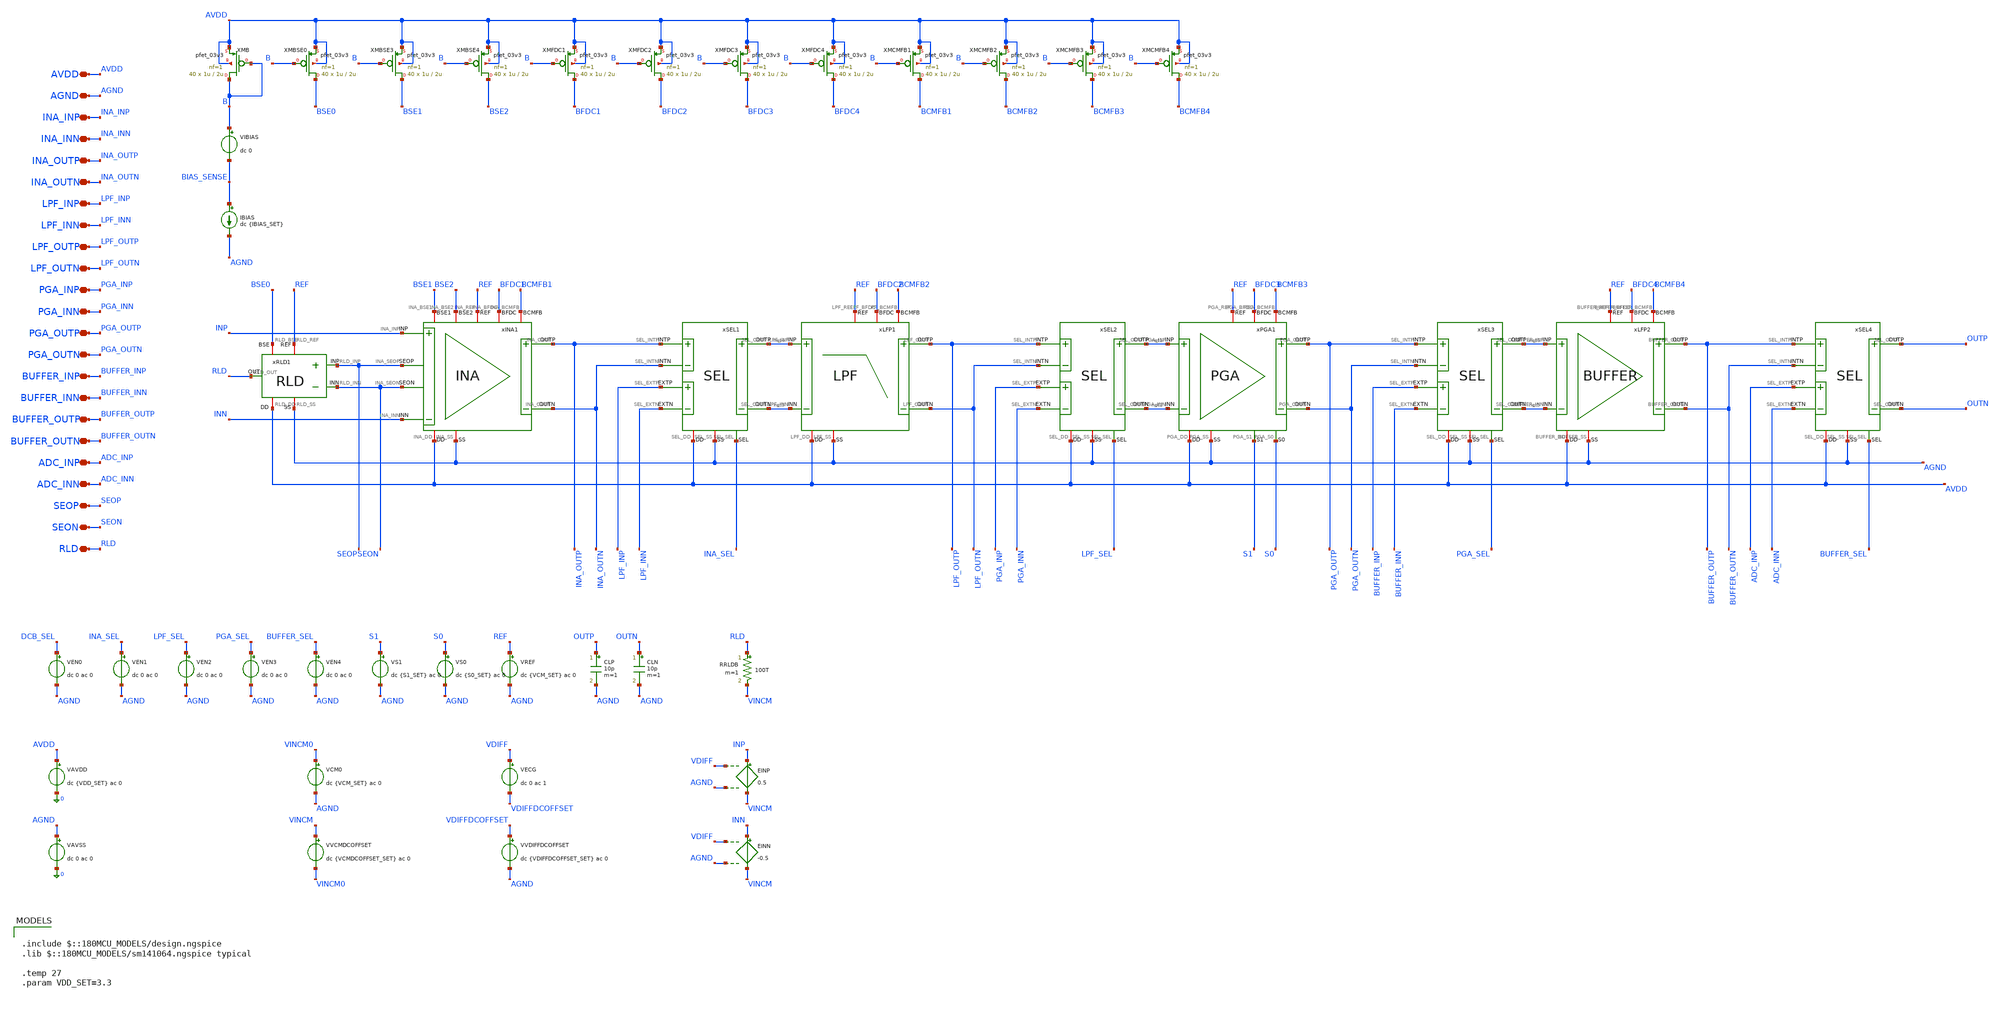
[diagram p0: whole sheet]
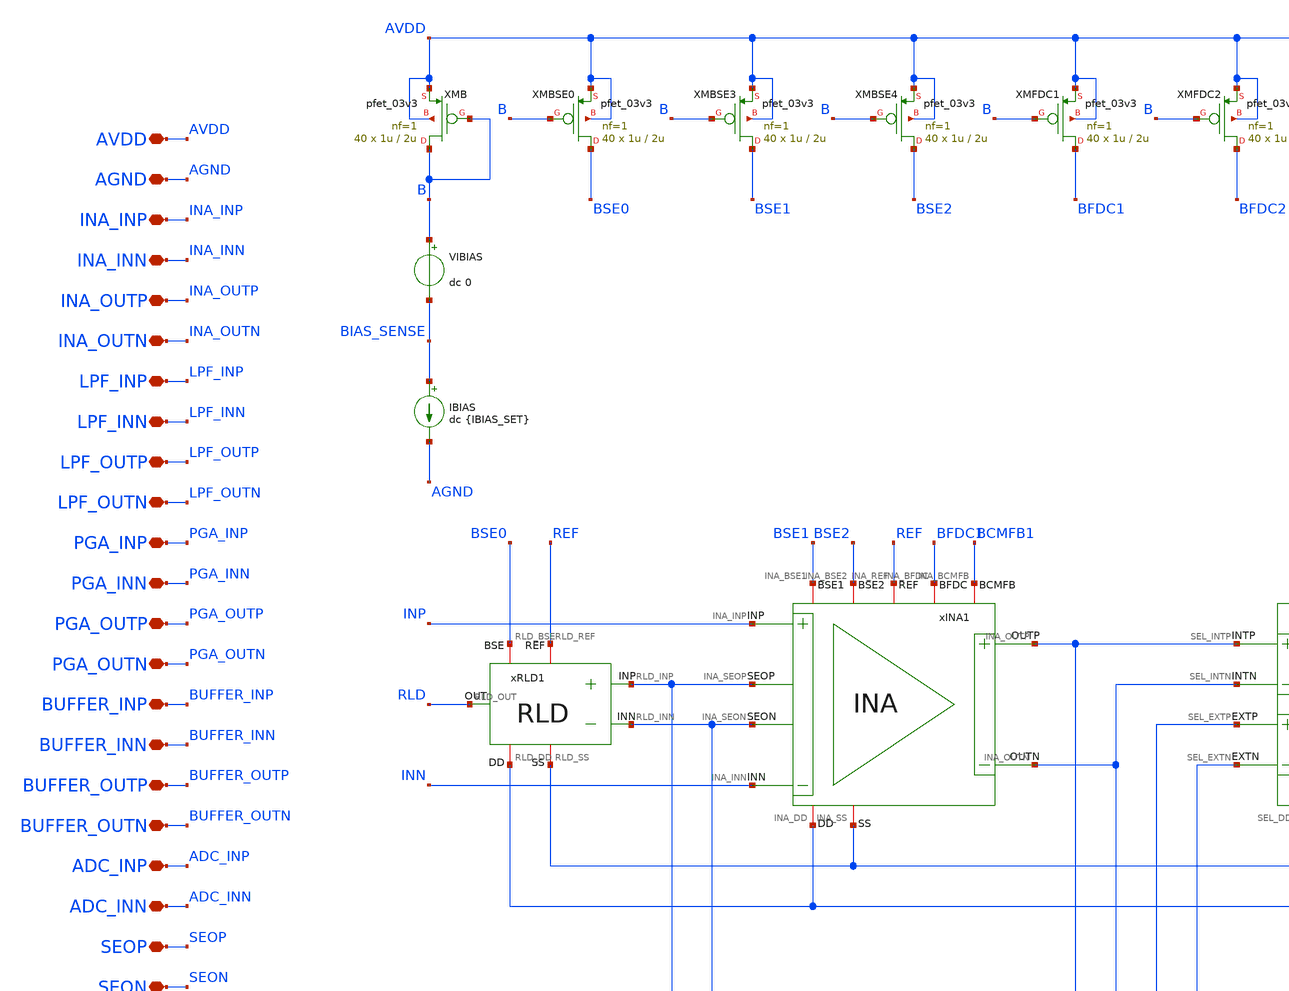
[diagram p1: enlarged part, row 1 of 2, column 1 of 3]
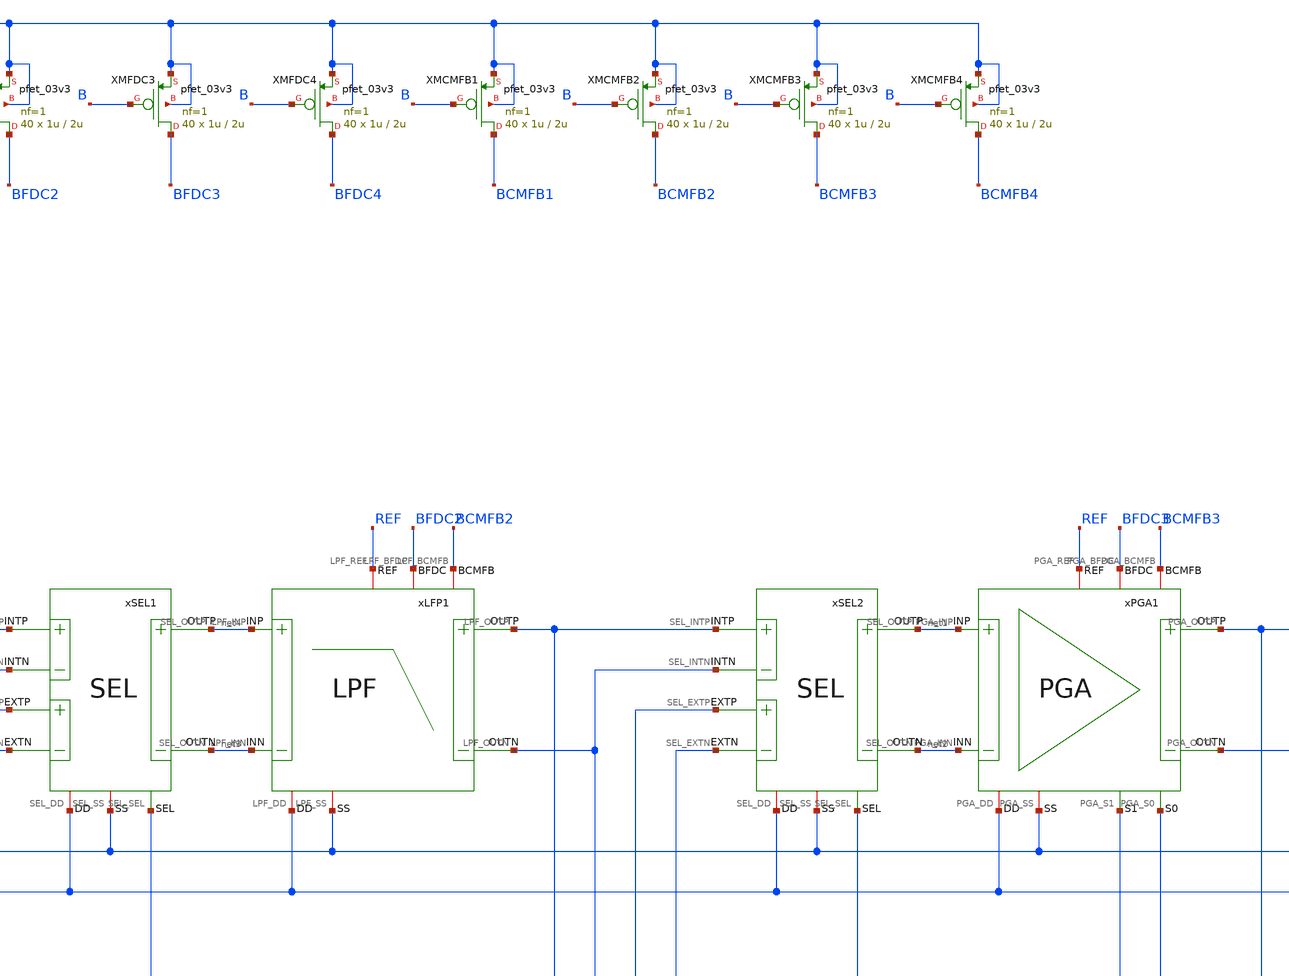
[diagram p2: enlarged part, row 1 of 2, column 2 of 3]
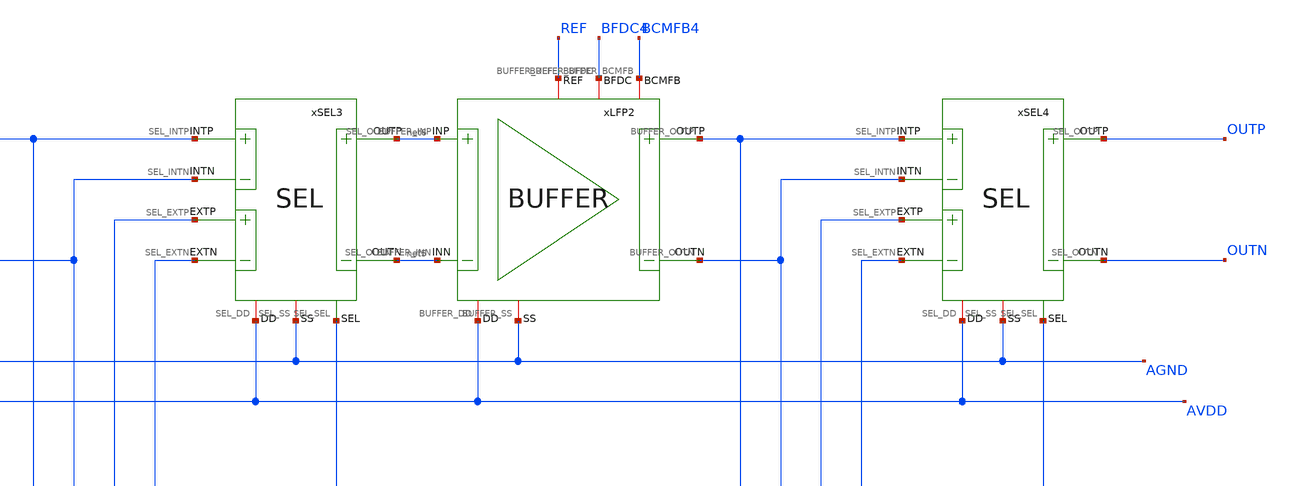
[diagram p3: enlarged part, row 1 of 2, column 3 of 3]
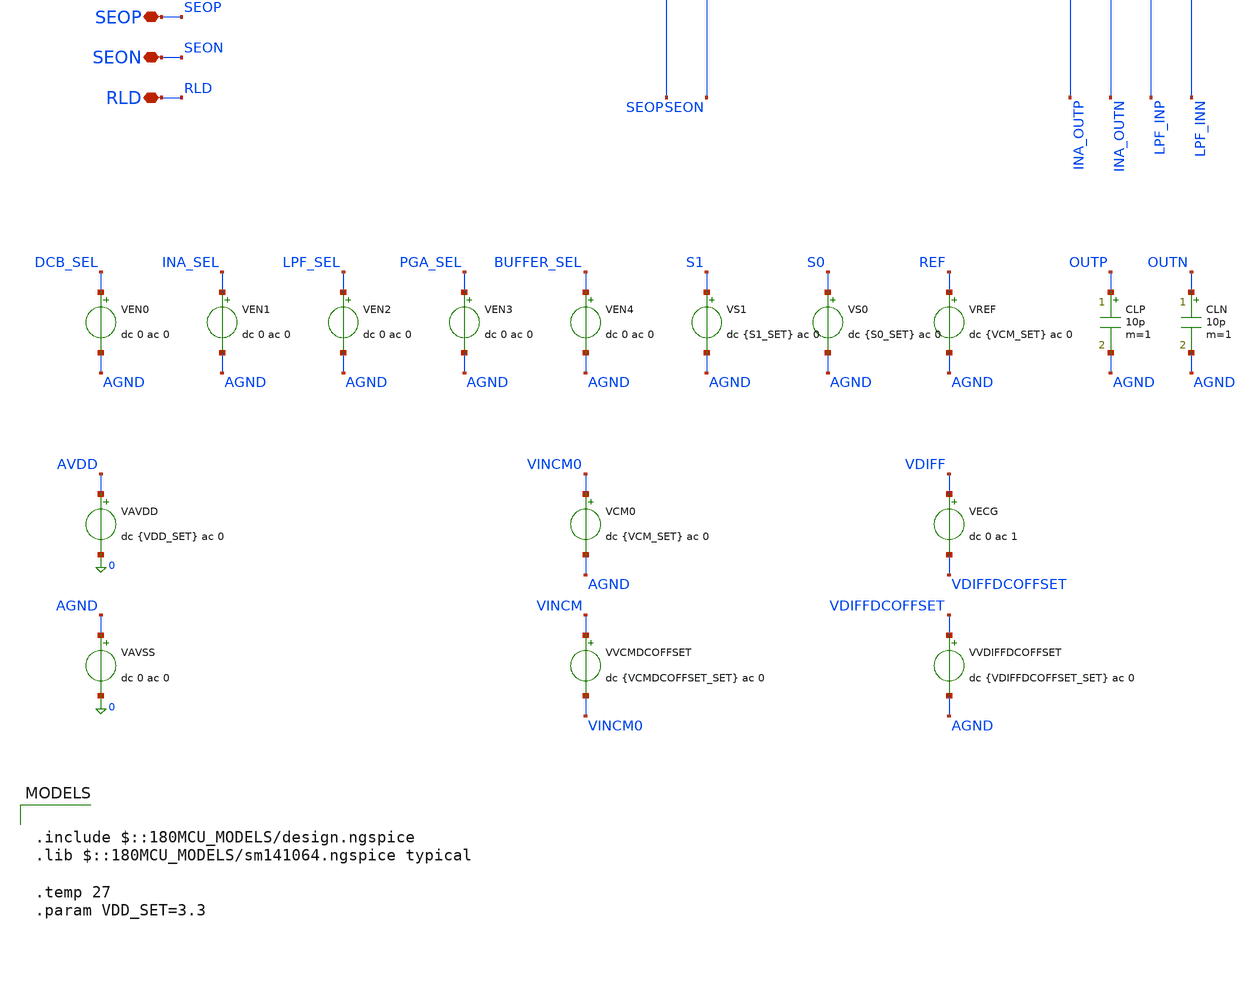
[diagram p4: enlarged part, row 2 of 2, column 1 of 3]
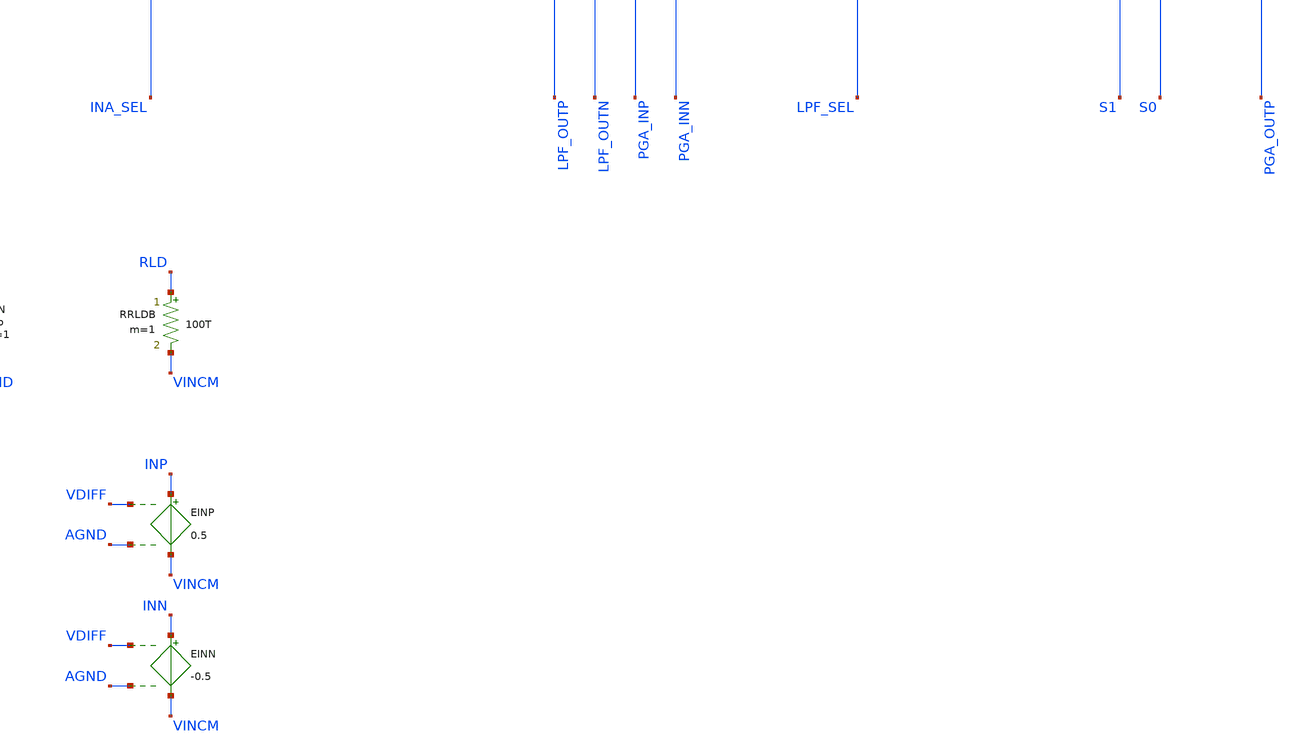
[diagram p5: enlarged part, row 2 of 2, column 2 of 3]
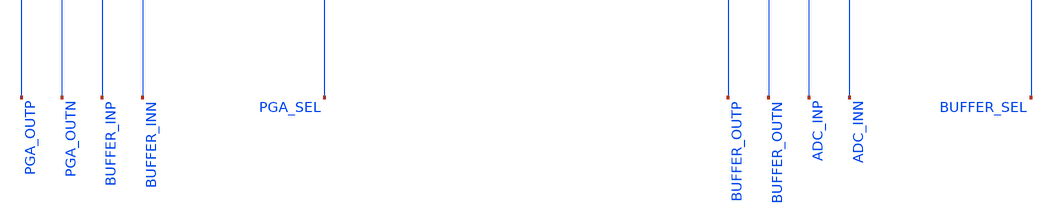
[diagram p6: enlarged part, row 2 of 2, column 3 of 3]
** sch_path: Design_Files/IC Design/Testbench/PATH/AC/PATH_TB_AC.sch
**.subckt PATH_TB_AC INA_INP INA_INN INA_OUTP INA_OUTN LPF_INP LPF_INN LPF_OUTP LPF_OUTN PGA_INP
*+ PGA_INN PGA_OUTP PGA_OUTN BUFFER_INP BUFFER_INN BUFFER_OUTP BUFFER_OUTN ADC_INP ADC_INN AVDD AGND SEOP SEON
*+ RLD
*.iopin INA_INP
*.iopin INA_INN
*.iopin INA_OUTP
*.iopin INA_OUTN
*.iopin LPF_INP
*.iopin LPF_INN
*.iopin LPF_OUTP
*.iopin LPF_OUTN
*.iopin PGA_INP
*.iopin PGA_INN
*.iopin PGA_OUTP
*.iopin PGA_OUTN
*.iopin BUFFER_INP
*.iopin BUFFER_INN
*.iopin BUFFER_OUTP
*.iopin BUFFER_OUTN
*.iopin ADC_INP
*.iopin ADC_INN
*.iopin AVDD
*.iopin AGND
*.iopin SEOP
*.iopin SEON
*.iopin RLD
CLP OUTP AGND 10p m=1
CLN OUTN AGND 10p m=1
VREF REF AGND dc {VCM_SET} ac 0
VEN1 INA_SEL AGND dc 0 ac 0
.save i(ven1)
VS0 S0 AGND dc {S0_SET} ac 0
VS1 S1 AGND dc {S1_SET} ac 0
VEN2 LPF_SEL AGND dc 0 ac 0
.save i(ven2)
VEN3 PGA_SEL AGND dc 0 ac 0
.save i(ven3)
VEN4 BUFFER_SEL AGND dc 0 ac 0
.save i(ven4)
VEN0 DCB_SEL AGND dc 0 ac 0
.save i(ven0)
VAVDD AVDD 0 dc {VDD_SET} ac 0
.save i(vavdd)
VAVSS AGND 0 dc 0 ac 0
.save i(vavss)
VCM0 VINCM0 AGND dc {VCM_SET} ac 0
VVCMDCOFFSET VINCM VINCM0 dc {VCMDCOFFSET_SET} ac 0
VECG VDIFF VDIFFDCOFFSET dc 0 ac 1
VVDIFFDCOFFSET VDIFFDCOFFSET AGND dc {VDIFFDCOFFSET_SET} ac 0
EINP INP VINCM VDIFF AGND 0.5
EINN INN VINCM VDIFF AGND -0.5
RRLDB RLD VINCM 100T m=1
VIBIAS B BIAS_SENSE dc 0
.save i(vibias)
IBIAS BIAS_SENSE AGND dc {IBIAS_SET}
xLFP1 AVDD AGND net4 net3 LPF_OUTN BFDC2 LPF_OUTP BCMFB2 REF LPF
xPGA1 AVDD AGND net1 net2 PGA_OUTN BFDC3 PGA_OUTP BCMFB3 REF S1 S0 PGA
xSEL1 AVDD AGND INA_OUTP INA_OUTN net3 net4 LPF_INP LPF_INN INA_SEL SEL
xINA1 AVDD AGND INP INN INA_OUTN BFDC1 INA_OUTP BCMFB1 REF SEON SEOP BSE1 BSE2 INA
xSEL2 AVDD AGND LPF_OUTP LPF_OUTN net2 net1 PGA_INP PGA_INN LPF_SEL SEL
xSEL3 AVDD AGND PGA_OUTP PGA_OUTN net5 net6 BUFFER_INP BUFFER_INN PGA_SEL SEL
xSEL4 AVDD AGND BUFFER_OUTP BUFFER_OUTN OUTN OUTP ADC_INP ADC_INN BUFFER_SEL SEL
xLFP2 AVDD AGND net6 net5 BUFFER_OUTN BFDC4 BUFFER_OUTP BCMFB4 REF BUFFER
XMB B B AVDD AVDD pfet_03v3 L=2u W=1u nf=1 ad='int((nf+1)/2) * W/nf * 0.18u' as='int((nf+2)/2) * W/nf * 0.18u'
+ pd='2*int((nf+1)/2) * (W/nf + 0.18u)' ps='2*int((nf+2)/2) * (W/nf + 0.18u)' nrd='0.18u / W' nrs='0.18u / W'
+ sa=0 sb=0 sd=0 m=40
XMBSE3 BSE1 B AVDD AVDD pfet_03v3 L=2u W=1u nf=1 ad='int((nf+1)/2) * W/nf * 0.18u' as='int((nf+2)/2) * W/nf * 0.18u'
+ pd='2*int((nf+1)/2) * (W/nf + 0.18u)' ps='2*int((nf+2)/2) * (W/nf + 0.18u)' nrd='0.18u / W' nrs='0.18u / W'
+ sa=0 sb=0 sd=0 m=40
XMBSE4 BSE2 B AVDD AVDD pfet_03v3 L=2u W=1u nf=1 ad='int((nf+1)/2) * W/nf * 0.18u' as='int((nf+2)/2) * W/nf * 0.18u'
+ pd='2*int((nf+1)/2) * (W/nf + 0.18u)' ps='2*int((nf+2)/2) * (W/nf + 0.18u)' nrd='0.18u / W' nrs='0.18u / W'
+ sa=0 sb=0 sd=0 m=40
XMFDC1 BFDC1 B AVDD AVDD pfet_03v3 L=2u W=1u nf=1 ad='int((nf+1)/2) * W/nf * 0.18u' as='int((nf+2)/2) * W/nf * 0.18u'
+ pd='2*int((nf+1)/2) * (W/nf + 0.18u)' ps='2*int((nf+2)/2) * (W/nf + 0.18u)' nrd='0.18u / W' nrs='0.18u / W'
+ sa=0 sb=0 sd=0 m=40
XMFDC2 BFDC2 B AVDD AVDD pfet_03v3 L=2u W=1u nf=1 ad='int((nf+1)/2) * W/nf * 0.18u' as='int((nf+2)/2) * W/nf * 0.18u'
+ pd='2*int((nf+1)/2) * (W/nf + 0.18u)' ps='2*int((nf+2)/2) * (W/nf + 0.18u)' nrd='0.18u / W' nrs='0.18u / W'
+ sa=0 sb=0 sd=0 m=40
XMFDC3 BFDC3 B AVDD AVDD pfet_03v3 L=2u W=1u nf=1 ad='int((nf+1)/2) * W/nf * 0.18u' as='int((nf+2)/2) * W/nf * 0.18u'
+ pd='2*int((nf+1)/2) * (W/nf + 0.18u)' ps='2*int((nf+2)/2) * (W/nf + 0.18u)' nrd='0.18u / W' nrs='0.18u / W'
+ sa=0 sb=0 sd=0 m=40
XMFDC4 BFDC4 B AVDD AVDD pfet_03v3 L=2u W=1u nf=1 ad='int((nf+1)/2) * W/nf * 0.18u' as='int((nf+2)/2) * W/nf * 0.18u'
+ pd='2*int((nf+1)/2) * (W/nf + 0.18u)' ps='2*int((nf+2)/2) * (W/nf + 0.18u)' nrd='0.18u / W' nrs='0.18u / W'
+ sa=0 sb=0 sd=0 m=40
XMCMFB1 BCMFB1 B AVDD AVDD pfet_03v3 L=2u W=1u nf=1 ad='int((nf+1)/2) * W/nf * 0.18u' as='int((nf+2)/2) * W/nf * 0.18u'
+ pd='2*int((nf+1)/2) * (W/nf + 0.18u)' ps='2*int((nf+2)/2) * (W/nf + 0.18u)' nrd='0.18u / W' nrs='0.18u / W'
+ sa=0 sb=0 sd=0 m=40
XMCMFB2 BCMFB2 B AVDD AVDD pfet_03v3 L=2u W=1u nf=1 ad='int((nf+1)/2) * W/nf * 0.18u' as='int((nf+2)/2) * W/nf * 0.18u'
+ pd='2*int((nf+1)/2) * (W/nf + 0.18u)' ps='2*int((nf+2)/2) * (W/nf + 0.18u)' nrd='0.18u / W' nrs='0.18u / W'
+ sa=0 sb=0 sd=0 m=40
XMCMFB3 BCMFB3 B AVDD AVDD pfet_03v3 L=2u W=1u nf=1 ad='int((nf+1)/2) * W/nf * 0.18u' as='int((nf+2)/2) * W/nf * 0.18u'
+ pd='2*int((nf+1)/2) * (W/nf + 0.18u)' ps='2*int((nf+2)/2) * (W/nf + 0.18u)' nrd='0.18u / W' nrs='0.18u / W'
+ sa=0 sb=0 sd=0 m=40
XMCMFB4 BCMFB4 B AVDD AVDD pfet_03v3 L=2u W=1u nf=1 ad='int((nf+1)/2) * W/nf * 0.18u' as='int((nf+2)/2) * W/nf * 0.18u'
+ pd='2*int((nf+1)/2) * (W/nf + 0.18u)' ps='2*int((nf+2)/2) * (W/nf + 0.18u)' nrd='0.18u / W' nrs='0.18u / W'
+ sa=0 sb=0 sd=0 m=40
XMBSE0 BSE0 B AVDD AVDD pfet_03v3 L=2u W=1u nf=1 ad='int((nf+1)/2) * W/nf * 0.18u' as='int((nf+2)/2) * W/nf * 0.18u'
+ pd='2*int((nf+1)/2) * (W/nf + 0.18u)' ps='2*int((nf+2)/2) * (W/nf + 0.18u)' nrd='0.18u / W' nrs='0.18u / W'
+ sa=0 sb=0 sd=0 m=40
xRLD1 AVDD AGND SEOP SEON RLD REF BSE0 RLD
**** begin user architecture code

.include $::180MCU_MODELS/design.ngspice
.lib $::180MCU_MODELS/sm141064.ngspice typical

.temp 27
.param VDD_SET=3.3



.param VCM_SET={VDD_SET/2}

.param VCMDCOFFSET_SET=0
.param VDIFFDCOFFSET_SET=0

.param IBIAS_SET=40u

.param S1_SET=3.3
.param S0_SET=3.3

.options method=gear
.options sparse

.options gmin=1e-12
.options rshunt=100T

.options reltol=1e-3
.options abstol=1e-12
.options vntol=1u
.options chgtol=1e-14

.options itl1=2000
.options itl2=1000
.options itl4=2000

.nodeset v(B)=2.3

.nodeset v(INP)={VCM_SET}
.nodeset v(INN)={VCM_SET}

.nodeset v(DCB_OUTP)={VCM_SET}
.nodeset v(DCB_OUTN)={VCM_SET}

.nodeset v(INA_OUTP)={VCM_SET}
.nodeset v(INA_OUTN)={VCM_SET}

.nodeset v(LPF_OUTP)={VCM_SET}
.nodeset v(LPF_OUTN)={VCM_SET}

.nodeset v(PGA_OUTP)={VCM_SET}
.nodeset v(PGA_OUTN)={VCM_SET}

.nodeset v(BUFFER_OUTP)={VCM_SET}
.nodeset v(BUFFER_OUTN)={VCM_SET}

.nodeset v(OUTP)={VCM_SET}
.nodeset v(OUTN)={VCM_SET}

.nodeset v(RLD)={VCM_SET}

.save all





.control

destroy all

set noaskquit
set wr_singlescale
unset wr_vecnames
set appendwrite
set units=degrees

option numdgt=15
option sparse

shell mkdir -p
+ /foss/designs/ECG_Acquisition_IC/Measurement_Results/IC_Simulation/PATH/NOM.Result_txt

shell rm -f
+ /foss/designs/ECG_Acquisition_IC/Measurement_Results/IC_Simulation/PATH/NOM.Result_txt/NOM.op.txt
shell rm -f
+ /foss/designs/ECG_Acquisition_IC/Measurement_Results/IC_Simulation/PATH/NOM.Result_txt/NOM.diff_ac.txt
shell rm -f
+ /foss/designs/ECG_Acquisition_IC/Measurement_Results/IC_Simulation/PATH/NOM.Result_txt/NOM.cmrr_ac.txt
shell rm -f
+ /foss/designs/ECG_Acquisition_IC/Measurement_Results/IC_Simulation/PATH/NOM.Result_txt/NOM.psrrp_ac.txt
shell rm -f
+ /foss/designs/ECG_Acquisition_IC/Measurement_Results/IC_Simulation/PATH/NOM.Result_txt/NOM.psrrn_ac.txt


* OP: G2 and G16
foreach gaincfg 0 1

    if $gaincfg = 0
        alterparam S1_SET=0
        alterparam S0_SET=0
    else
        alterparam S1_SET=3.3
        alterparam S0_SET=3.3
    end

    reset
    save all

    alter @VECG[ACMAG]=0
    alter @VECG[ACPHASE]=0

    alter @VCM0[ACMAG]=0
    alter @VCM0[ACPHASE]=0

    alter @VAVDD[ACMAG]=0
    alter @VAVDD[ACPHASE]=0

    alter @VAVSS[ACMAG]=0
    alter @VAVSS[ACPHASE]=0

    op

    let op_index=0

    if $gaincfg = 0
        let op_pga_gain=op_index*0+2
    else
        let op_pga_gain=op_index*0+16
    end

    let op_vdd=v(AVDD)-v(AGND)

    let op_vinp=v(INP)-v(AGND)
    let op_vinn=v(INN)-v(AGND)

    let op_vin_cm=0.5*(v(INP)+v(INN))-v(AGND)
    let op_vin_diff=v(INP)-v(INN)

    let op_outp=v(OUTP)-v(AGND)
    let op_outn=v(OUTN)-v(AGND)

    let op_vout_cm=0.5*(v(OUTP)+v(OUTN))-v(AGND)
    let op_vout_diff=v(OUTP)-v(OUTN)

    let op_rld=v(RLD)-v(AGND)
    let op_ref=v(REF)-v(AGND)

    let op_ibias=abs(vibias#branch)
    let op_idd=abs(vavdd#branch)
    let op_power=op_vdd*op_idd

    setscale op_index

    wrdata
+ /foss/designs/ECG_Acquisition_IC/Measurement_Results/IC_Simulation/PATH/NOM.Result_txt/NOM.op.txt op_pga_gain op_vdd op_vinp op_vinn op_vin_cm op_vin_diff op_outp op_outn op_vout_cm op_vout_diff
+ op_rld op_ref op_ibias op_idd op_power

    destroy $curplot

end


* Differential AC: G2 and G16
foreach gaincfg 0 1

    if $gaincfg = 0
        alterparam S1_SET=0
        alterparam S0_SET=0
    else
        alterparam S1_SET=3.3
        alterparam S0_SET=3.3
    end

    reset
    save all

    alter @VECG[ACMAG]=1
    alter @VECG[ACPHASE]=0

    alter @VCM0[ACMAG]=0
    alter @VCM0[ACPHASE]=0

    alter @VAVDD[ACMAG]=0
    alter @VAVDD[ACPHASE]=0

    alter @VAVSS[ACMAG]=0
    alter @VAVSS[ACPHASE]=0

    ac dec 200 0.001 10k

    if $gaincfg = 0
        let ac_pga_gain=frequency*0+2
    else
        let ac_pga_gain=frequency*0+16
    end

    let ac_vin_diff=v(INP)-v(INN)
    let ac_vout_diff=v(OUTP)-v(OUTN)
    let ac_vout_cm=0.5*(v(OUTP)+v(OUTN))-v(AGND)

    let ac_hdiff=ac_vout_diff/ac_vin_diff

    let vin_diff_real=real(ac_vin_diff)
    let vin_diff_imag=imag(ac_vin_diff)
    let vin_diff_mag=mag(ac_vin_diff)
    let vin_diff_phase=ph(ac_vin_diff)

    let vout_diff_real=real(ac_vout_diff)
    let vout_diff_imag=imag(ac_vout_diff)
    let vout_diff_mag=mag(ac_vout_diff)
    let vout_diff_phase=ph(ac_vout_diff)

    let vout_cm_real=real(ac_vout_cm)
    let vout_cm_imag=imag(ac_vout_cm)

    let hdiff_real=real(ac_hdiff)
    let hdiff_imag=imag(ac_hdiff)
    let hdiff_mag=mag(ac_hdiff)
    let hdiff_db=db(ac_hdiff)
    let hdiff_phase=ph(ac_hdiff)

    setscale frequency

    wrdata
+ /foss/designs/ECG_Acquisition_IC/Measurement_Results/IC_Simulation/PATH/NOM.Result_txt/NOM.diff_ac.txt ac_pga_gain vin_diff_real vin_diff_imag vin_diff_mag vin_diff_phase vout_diff_real vout_diff_imag
+ vout_diff_mag vout_diff_phase vout_cm_real vout_cm_imag hdiff_real hdiff_imag hdiff_mag hdiff_db hdiff_phase

    destroy $curplot

end


* CMRR AC: G2 and G16
foreach gaincfg 0 1

    if $gaincfg = 0
        alterparam S1_SET=0
        alterparam S0_SET=0
    else
        alterparam S1_SET=3.3
        alterparam S0_SET=3.3
    end

    reset
    save all

    alter @VECG[ACMAG]=0
    alter @VECG[ACPHASE]=0

    alter @VCM0[ACMAG]=1
    alter @VCM0[ACPHASE]=0

    alter @VAVDD[ACMAG]=0
    alter @VAVDD[ACPHASE]=0

    alter @VAVSS[ACMAG]=0
    alter @VAVSS[ACPHASE]=0

    ac dec 200 0.001 10k

    if $gaincfg = 0
        let ac_pga_gain=frequency*0+2
    else
        let ac_pga_gain=frequency*0+16
    end

    let ac_vin_cm=0.5*(v(INP)+v(INN))-v(AGND)
    let ac_vout_diff=v(OUTP)-v(OUTN)
    let ac_vout_cm=0.5*(v(OUTP)+v(OUTN))-v(AGND)

    let ac_hcm_diff=ac_vout_diff/ac_vin_cm

    let vin_cm_real=real(ac_vin_cm)
    let vin_cm_imag=imag(ac_vin_cm)
    let vin_cm_mag=mag(ac_vin_cm)
    let vin_cm_phase=ph(ac_vin_cm)

    let vout_diff_real=real(ac_vout_diff)
    let vout_diff_imag=imag(ac_vout_diff)

    let vout_cm_real=real(ac_vout_cm)
    let vout_cm_imag=imag(ac_vout_cm)

    let hcm_diff_real=real(ac_hcm_diff)
    let hcm_diff_imag=imag(ac_hcm_diff)
    let hcm_diff_mag=mag(ac_hcm_diff)
    let hcm_diff_db=db(ac_hcm_diff)
    let hcm_diff_phase=ph(ac_hcm_diff)

    setscale frequency

    wrdata
+ /foss/designs/ECG_Acquisition_IC/Measurement_Results/IC_Simulation/PATH/NOM.Result_txt/NOM.cmrr_ac.txt ac_pga_gain vin_cm_real vin_cm_imag vin_cm_mag vin_cm_phase vout_diff_real vout_diff_imag
+ vout_cm_real vout_cm_imag hcm_diff_real hcm_diff_imag hcm_diff_mag hcm_diff_db hcm_diff_phase

    destroy $curplot

end


* PSRR+ AC: G2 and G16
foreach gaincfg 0 1

    if $gaincfg = 0
        alterparam S1_SET=0
        alterparam S0_SET=0
    else
        alterparam S1_SET=3.3
        alterparam S0_SET=3.3
    end

    reset
    save all

    alter @VECG[ACMAG]=0
    alter @VECG[ACPHASE]=0

    alter @VCM0[ACMAG]=0
    alter @VCM0[ACPHASE]=0

    alter @VAVDD[ACMAG]=1
    alter @VAVDD[ACPHASE]=0

    alter @VAVSS[ACMAG]=0
    alter @VAVSS[ACPHASE]=0

    ac dec 200 0.001 10k

    if $gaincfg = 0
        let ac_pga_gain=frequency*0+2
    else
        let ac_pga_gain=frequency*0+16
    end

    let ac_supply=v(AVDD)-v(AGND)
    let ac_vout_diff=v(OUTP)-v(OUTN)
    let ac_vout_cm=0.5*(v(OUTP)+v(OUTN))-v(AGND)

    let ac_hpsrrp=ac_vout_diff/ac_supply

    let supply_real=real(ac_supply)
    let supply_imag=imag(ac_supply)
    let supply_mag=mag(ac_supply)
    let supply_phase=ph(ac_supply)

    let vout_diff_real=real(ac_vout_diff)
    let vout_diff_imag=imag(ac_vout_diff)

    let vout_cm_real=real(ac_vout_cm)
    let vout_cm_imag=imag(ac_vout_cm)

    let hpsrrp_real=real(ac_hpsrrp)
    let hpsrrp_imag=imag(ac_hpsrrp)
    let hpsrrp_mag=mag(ac_hpsrrp)
    let hpsrrp_db=db(ac_hpsrrp)
    let hpsrrp_phase=ph(ac_hpsrrp)

    setscale frequency

    wrdata
+ /foss/designs/ECG_Acquisition_IC/Measurement_Results/IC_Simulation/PATH/NOM.Result_txt/NOM.psrrp_ac.txt ac_pga_gain supply_real supply_imag supply_mag supply_phase vout_diff_real vout_diff_imag
+ vout_cm_real vout_cm_imag hpsrrp_real hpsrrp_imag hpsrrp_mag hpsrrp_db hpsrrp_phase

    destroy $curplot

end


* PSRR- AC: G2 and G16
foreach gaincfg 0 1

    if $gaincfg = 0
        alterparam S1_SET=0
        alterparam S0_SET=0
    else
        alterparam S1_SET=3.3
        alterparam S0_SET=3.3
    end

    reset
    save all

    alter @VECG[ACMAG]=0
    alter @VECG[ACPHASE]=0

    alter @VCM0[ACMAG]=0
    alter @VCM0[ACPHASE]=0

    alter @VAVDD[ACMAG]=0
    alter @VAVDD[ACPHASE]=0

    alter @VAVSS[ACMAG]=1
    alter @VAVSS[ACPHASE]=0

    ac dec 200 0.001 10k

    if $gaincfg = 0
        let ac_pga_gain=frequency*0+2
    else
        let ac_pga_gain=frequency*0+16
    end

    let ac_supply=v(AGND)
    let ac_vout_diff=v(OUTP)-v(OUTN)
    let ac_vout_cm=0.5*(v(OUTP)+v(OUTN))-v(AGND)

    let ac_hpsrrn=ac_vout_diff/ac_supply

    let supply_real=real(ac_supply)
    let supply_imag=imag(ac_supply)
    let supply_mag=mag(ac_supply)
    let supply_phase=ph(ac_supply)

    let vout_diff_real=real(ac_vout_diff)
    let vout_diff_imag=imag(ac_vout_diff)

    let vout_cm_real=real(ac_vout_cm)
    let vout_cm_imag=imag(ac_vout_cm)

    let hpsrrn_real=real(ac_hpsrrn)
    let hpsrrn_imag=imag(ac_hpsrrn)
    let hpsrrn_mag=mag(ac_hpsrrn)
    let hpsrrn_db=db(ac_hpsrrn)
    let hpsrrn_phase=ph(ac_hpsrrn)

    setscale frequency

    wrdata
+ /foss/designs/ECG_Acquisition_IC/Measurement_Results/IC_Simulation/PATH/NOM.Result_txt/NOM.psrrn_ac.txt ac_pga_gain supply_real supply_imag supply_mag supply_phase vout_diff_real vout_diff_imag
+ vout_cm_real vout_cm_imag hpsrrn_real hpsrrn_imag hpsrrn_mag hpsrrn_db hpsrrn_phase

    destroy $curplot

end


* Last simulated gain is already G16

quit
.endc


**** end user architecture code
**.ends
.end
